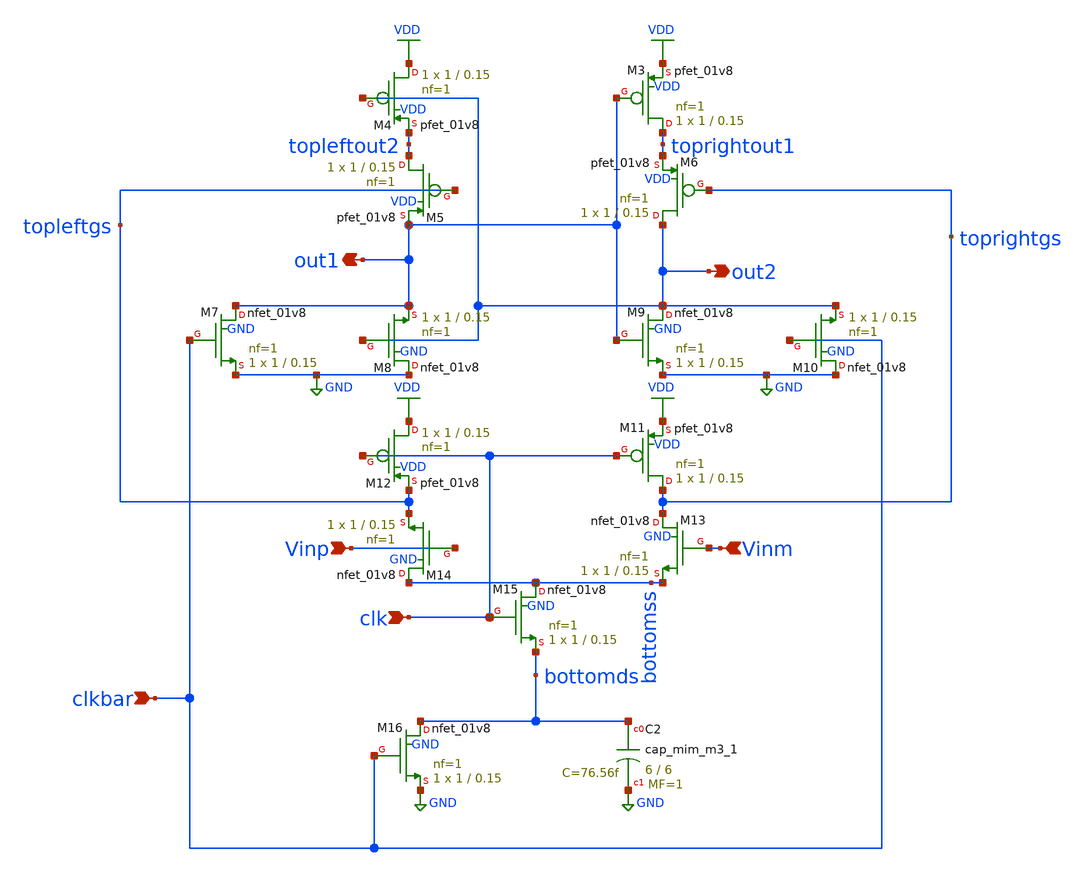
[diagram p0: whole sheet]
** sch_path: xschem/comparator/doubletaillatchforLVS.sch
**.subckt doubletaillatchforLVS clkbar out1 Vinp Vinm clk out2
*.ipin clkbar
*.opin out1
*.ipin Vinp
*.ipin Vinm
*.ipin clk
*.opin out2
XM3 toprightout1 out1 VDD VDD sky130_fd_pr__pfet_01v8 L=0.15 W=1 nf=1 ad='int((nf+1)/2) * W/nf * 0.29'
+ as='int((nf+2)/2) * W/nf * 0.29' pd='2*int((nf+1)/2) * (W/nf + 0.29)' ps='2*int((nf+2)/2) * (W/nf + 0.29)'
+ nrd='0.29 / W' nrs='0.29 / W' sa=0 sb=0 sd=0 mult=1 m=1
XM4 VDD out2 topleftout2 VDD sky130_fd_pr__pfet_01v8 L=0.15 W=1 nf=1 ad='int((nf+1)/2) * W/nf * 0.29'
+ as='int((nf+2)/2) * W/nf * 0.29' pd='2*int((nf+1)/2) * (W/nf + 0.29)' ps='2*int((nf+2)/2) * (W/nf + 0.29)'
+ nrd='0.29 / W' nrs='0.29 / W' sa=0 sb=0 sd=0 mult=1 m=1
XM5 topleftout2 topleftgs out1 VDD sky130_fd_pr__pfet_01v8 L=0.15 W=1 nf=1 ad='int((nf+1)/2) * W/nf * 0.29'
+ as='int((nf+2)/2) * W/nf * 0.29' pd='2*int((nf+1)/2) * (W/nf + 0.29)' ps='2*int((nf+2)/2) * (W/nf + 0.29)'
+ nrd='0.29 / W' nrs='0.29 / W' sa=0 sb=0 sd=0 mult=1 m=1
XM6 out2 toprightgs toprightout1 VDD sky130_fd_pr__pfet_01v8 L=0.15 W=1 nf=1 ad='int((nf+1)/2) * W/nf * 0.29'
+ as='int((nf+2)/2) * W/nf * 0.29' pd='2*int((nf+1)/2) * (W/nf + 0.29)' ps='2*int((nf+2)/2) * (W/nf + 0.29)'
+ nrd='0.29 / W' nrs='0.29 / W' sa=0 sb=0 sd=0 mult=1 m=1
XM7 out1 clkbar GND GND sky130_fd_pr__nfet_01v8 L=0.15 W=1 nf=1 ad='int((nf+1)/2) * W/nf * 0.29' as='int((nf+2)/2) * W/nf * 0.29'
+ pd='2*int((nf+1)/2) * (W/nf + 0.29)' ps='2*int((nf+2)/2) * (W/nf + 0.29)' nrd='0.29 / W' nrs='0.29 / W'
+ sa=0 sb=0 sd=0 mult=1 m=1
XM8 GND out2 out1 GND sky130_fd_pr__nfet_01v8 L=0.15 W=1 nf=1 ad='int((nf+1)/2) * W/nf * 0.29' as='int((nf+2)/2) * W/nf * 0.29'
+ pd='2*int((nf+1)/2) * (W/nf + 0.29)' ps='2*int((nf+2)/2) * (W/nf + 0.29)' nrd='0.29 / W' nrs='0.29 / W'
+ sa=0 sb=0 sd=0 mult=1 m=1
XM9 out2 out1 GND GND sky130_fd_pr__nfet_01v8 L=0.15 W=1 nf=1 ad='int((nf+1)/2) * W/nf * 0.29' as='int((nf+2)/2) * W/nf * 0.29'
+ pd='2*int((nf+1)/2) * (W/nf + 0.29)' ps='2*int((nf+2)/2) * (W/nf + 0.29)' nrd='0.29 / W' nrs='0.29 / W'
+ sa=0 sb=0 sd=0 mult=1 m=1
XM10 GND clkbar out2 GND sky130_fd_pr__nfet_01v8 L=0.15 W=1 nf=1 ad='int((nf+1)/2) * W/nf * 0.29' as='int((nf+2)/2) * W/nf * 0.29'
+ pd='2*int((nf+1)/2) * (W/nf + 0.29)' ps='2*int((nf+2)/2) * (W/nf + 0.29)' nrd='0.29 / W' nrs='0.29 / W'
+ sa=0 sb=0 sd=0 mult=1 m=1
XM11 toprightgs clk VDD VDD sky130_fd_pr__pfet_01v8 L=0.15 W=1 nf=1 ad='int((nf+1)/2) * W/nf * 0.29'
+ as='int((nf+2)/2) * W/nf * 0.29' pd='2*int((nf+1)/2) * (W/nf + 0.29)' ps='2*int((nf+2)/2) * (W/nf + 0.29)'
+ nrd='0.29 / W' nrs='0.29 / W' sa=0 sb=0 sd=0 mult=1 m=1
XM12 VDD clk topleftgs VDD sky130_fd_pr__pfet_01v8 L=0.15 W=1 nf=1 ad='int((nf+1)/2) * W/nf * 0.29' as='int((nf+2)/2) * W/nf * 0.29'
+ pd='2*int((nf+1)/2) * (W/nf + 0.29)' ps='2*int((nf+2)/2) * (W/nf + 0.29)' nrd='0.29 / W' nrs='0.29 / W'
+ sa=0 sb=0 sd=0 mult=1 m=1
XM13 toprightgs Vinm bottomss GND sky130_fd_pr__nfet_01v8 L=0.15 W=1 nf=1 ad='int((nf+1)/2) * W/nf * 0.29'
+ as='int((nf+2)/2) * W/nf * 0.29' pd='2*int((nf+1)/2) * (W/nf + 0.29)' ps='2*int((nf+2)/2) * (W/nf + 0.29)'
+ nrd='0.29 / W' nrs='0.29 / W' sa=0 sb=0 sd=0 mult=1 m=1
XM14 bottomss Vinp topleftgs GND sky130_fd_pr__nfet_01v8 L=0.15 W=1 nf=1 ad='int((nf+1)/2) * W/nf * 0.29'
+ as='int((nf+2)/2) * W/nf * 0.29' pd='2*int((nf+1)/2) * (W/nf + 0.29)' ps='2*int((nf+2)/2) * (W/nf + 0.29)'
+ nrd='0.29 / W' nrs='0.29 / W' sa=0 sb=0 sd=0 mult=1 m=1
XM15 bottomss clk bottomds GND sky130_fd_pr__nfet_01v8 L=0.15 W=1 nf=1 ad='int((nf+1)/2) * W/nf * 0.29'
+ as='int((nf+2)/2) * W/nf * 0.29' pd='2*int((nf+1)/2) * (W/nf + 0.29)' ps='2*int((nf+2)/2) * (W/nf + 0.29)'
+ nrd='0.29 / W' nrs='0.29 / W' sa=0 sb=0 sd=0 mult=1 m=1
XM16 bottomds clkbar GND GND sky130_fd_pr__nfet_01v8 L=0.15 W=1 nf=1 ad='int((nf+1)/2) * W/nf * 0.29'
+ as='int((nf+2)/2) * W/nf * 0.29' pd='2*int((nf+1)/2) * (W/nf + 0.29)' ps='2*int((nf+2)/2) * (W/nf + 0.29)'
+ nrd='0.29 / W' nrs='0.29 / W' sa=0 sb=0 sd=0 mult=1 m=1
XC2 bottomds GND sky130_fd_pr__cap_mim_m3_1 W=6 L=6 MF=1 m=1
**.ends
.GLOBAL VDD
.GLOBAL GND
.end
